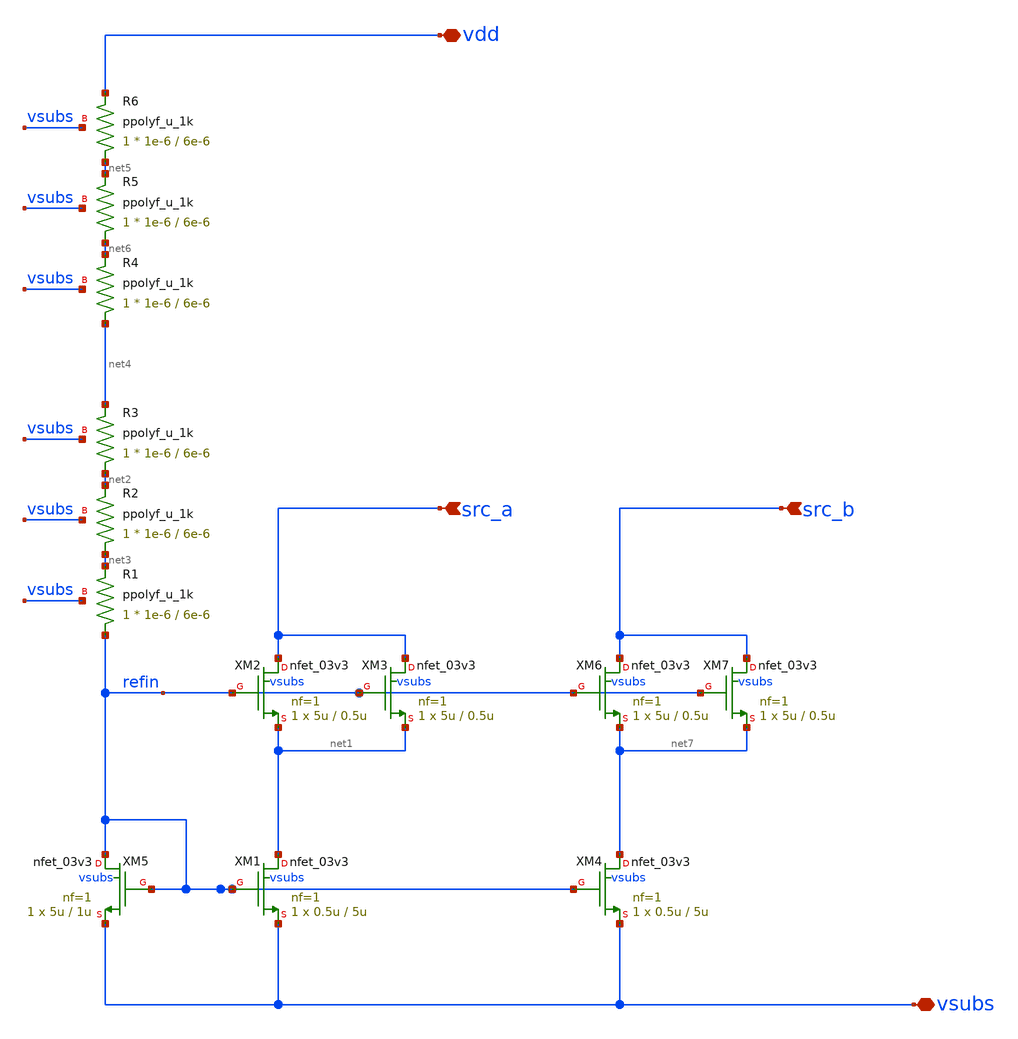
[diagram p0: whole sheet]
** sch_path: xschem/ip_current_source.sch
**.subckt ip_current_source vdd vsubs src_a src_b
*.iopin vdd
*.iopin vsubs
*.ipin src_a
*.ipin src_b
XR1 refin net3 vsubs ppolyf_u_1k r_width=1e-6 r_length=6e-6 m=1
XR2 net3 net2 vsubs ppolyf_u_1k r_width=1e-6 r_length=6e-6 m=1
XR3 net2 net4 vsubs ppolyf_u_1k r_width=1e-6 r_length=6e-6 m=1
XR4 net4 net6 vsubs ppolyf_u_1k r_width=1e-6 r_length=6e-6 m=1
XR5 net6 net5 vsubs ppolyf_u_1k r_width=1e-6 r_length=6e-6 m=1
XR6 net5 vdd vsubs ppolyf_u_1k r_width=1e-6 r_length=6e-6 m=1
XM5 refin refin vsubs vsubs nfet_03v3 L=1u W=5u nf=1 ad='int((nf+1)/2) * W/nf * 0.18u' as='int((nf+2)/2) * W/nf * 0.18u'
+ pd='2*int((nf+1)/2) * (W/nf + 0.18u)' ps='2*int((nf+2)/2) * (W/nf + 0.18u)' nrd='0.18u / W' nrs='0.18u / W'
+ sa=0 sb=0 sd=0 m=1 par=1
XM1 net1 refin vsubs vsubs nfet_03v3 L=5u W=0.5u nf=1 ad='int((nf+1)/2) * W/nf * 0.18u' as='int((nf+2)/2) * W/nf * 0.18u'
+ pd='2*int((nf+1)/2) * (W/nf + 0.18u)' ps='2*int((nf+2)/2) * (W/nf + 0.18u)' nrd='0.18u / W' nrs='0.18u / W'
+ sa=0 sb=0 sd=0 m=1 par=1
XM2 src_a refin net1 vsubs nfet_03v3 L=0.5u W=5u nf=1 ad='int((nf+1)/2) * W/nf * 0.18u' as='int((nf+2)/2) * W/nf * 0.18u'
+ pd='2*int((nf+1)/2) * (W/nf + 0.18u)' ps='2*int((nf+2)/2) * (W/nf + 0.18u)' nrd='0.18u / W' nrs='0.18u / W'
+ sa=0 sb=0 sd=0 m=1 par=1
XM3 src_a refin net1 vsubs nfet_03v3 L=0.5u W=5u nf=1 ad='int((nf+1)/2) * W/nf * 0.18u' as='int((nf+2)/2) * W/nf * 0.18u'
+ pd='2*int((nf+1)/2) * (W/nf + 0.18u)' ps='2*int((nf+2)/2) * (W/nf + 0.18u)' nrd='0.18u / W' nrs='0.18u / W'
+ sa=0 sb=0 sd=0 m=1 par=1
XM4 net7 refin vsubs vsubs nfet_03v3 L=5u W=0.5u nf=1 ad='int((nf+1)/2) * W/nf * 0.18u' as='int((nf+2)/2) * W/nf * 0.18u'
+ pd='2*int((nf+1)/2) * (W/nf + 0.18u)' ps='2*int((nf+2)/2) * (W/nf + 0.18u)' nrd='0.18u / W' nrs='0.18u / W'
+ sa=0 sb=0 sd=0 m=1 par=1
XM6 src_b refin net7 vsubs nfet_03v3 L=0.5u W=5u nf=1 ad='int((nf+1)/2) * W/nf * 0.18u' as='int((nf+2)/2) * W/nf * 0.18u'
+ pd='2*int((nf+1)/2) * (W/nf + 0.18u)' ps='2*int((nf+2)/2) * (W/nf + 0.18u)' nrd='0.18u / W' nrs='0.18u / W'
+ sa=0 sb=0 sd=0 m=1 par=1
XM7 src_b refin net7 vsubs nfet_03v3 L=0.5u W=5u nf=1 ad='int((nf+1)/2) * W/nf * 0.18u' as='int((nf+2)/2) * W/nf * 0.18u'
+ pd='2*int((nf+1)/2) * (W/nf + 0.18u)' ps='2*int((nf+2)/2) * (W/nf + 0.18u)' nrd='0.18u / W' nrs='0.18u / W'
+ sa=0 sb=0 sd=0 m=1 par=1
**.ends
.end
